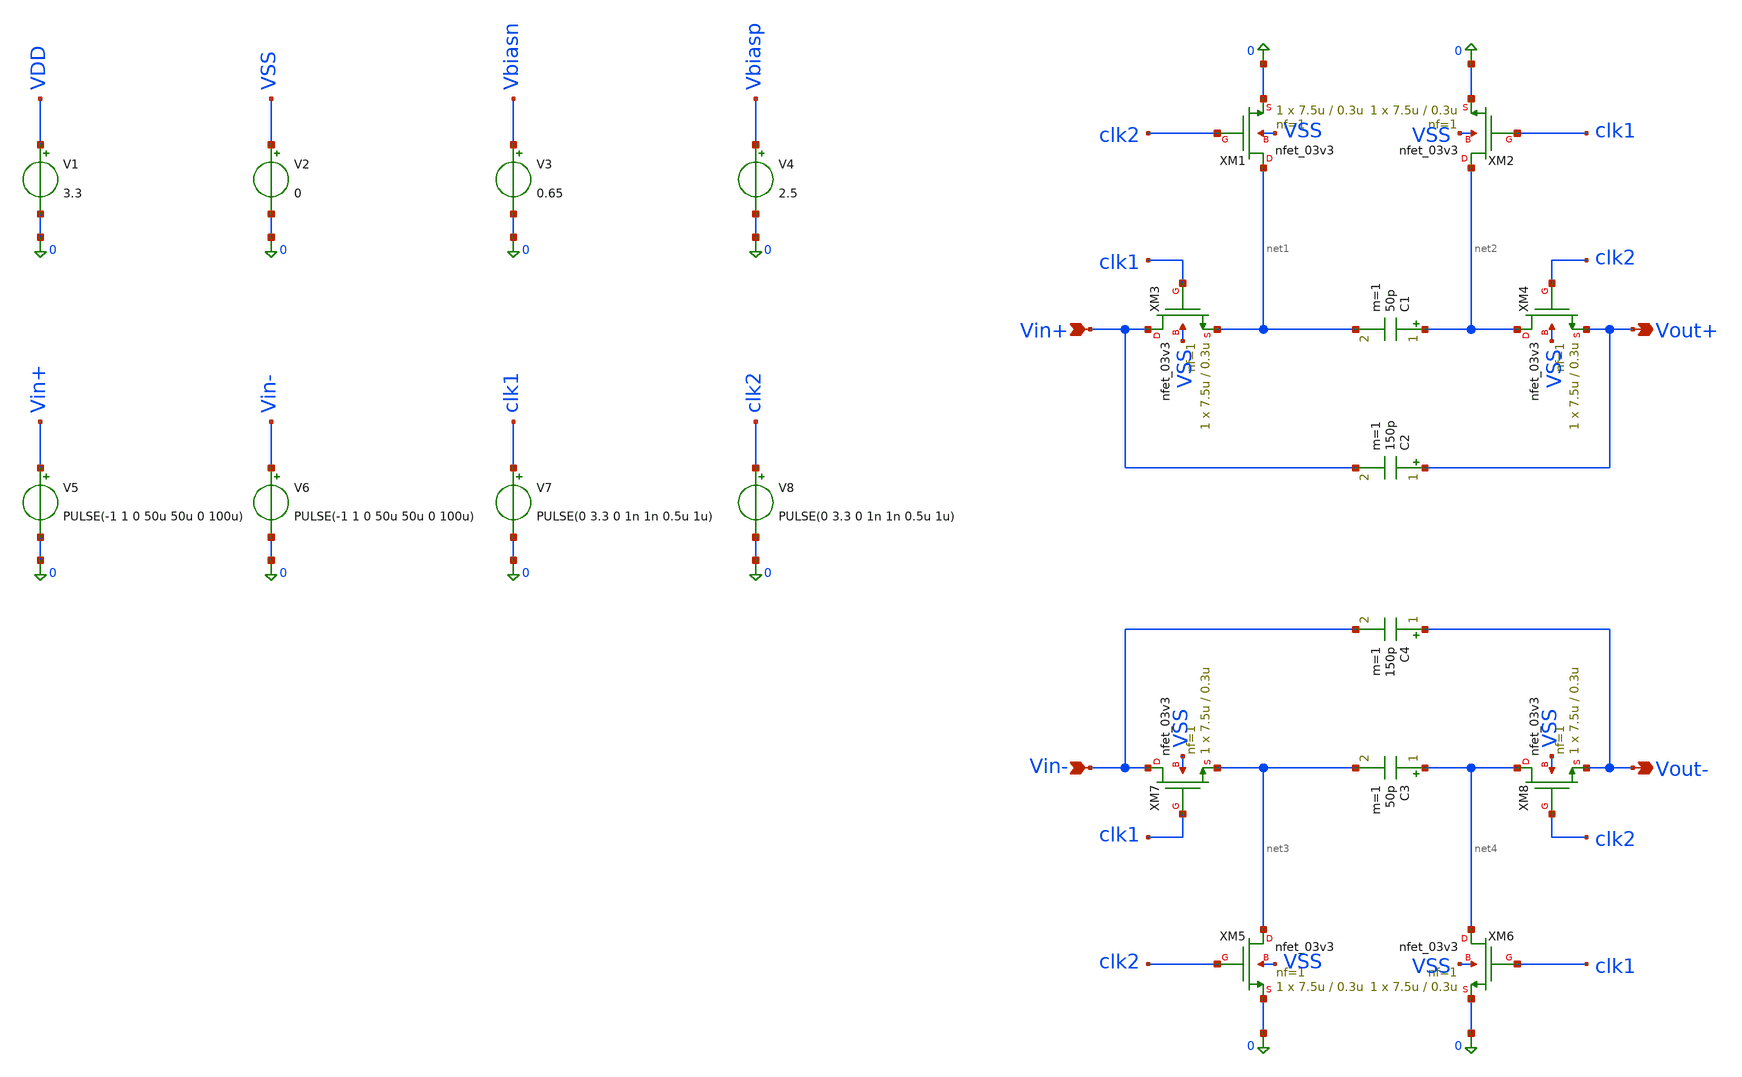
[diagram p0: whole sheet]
** sch_path: src/schematics/integrator_first_order/integrator.sch
**.subckt integrator Vin+ Vin- Vout+ Vout-
*.ipin Vin+
*.ipin Vin-
*.opin Vout+
*.opin Vout-
XM1 net1 clk2 0 VSS nfet_03v3 L=0.3u W=7.5u nf=1 ad='int((nf+1)/2) * W/nf * 0.18u' as='int((nf+2)/2) * W/nf * 0.18u'
+ pd='2*int((nf+1)/2) * (W/nf + 0.18u)' ps='2*int((nf+2)/2) * (W/nf + 0.18u)' nrd='0.18u / W' nrs='0.18u / W'
+ sa=0 sb=0 sd=0 m=1
XM2 net2 clk1 0 VSS nfet_03v3 L=0.3u W=7.5u nf=1 ad='int((nf+1)/2) * W/nf * 0.18u' as='int((nf+2)/2) * W/nf * 0.18u'
+ pd='2*int((nf+1)/2) * (W/nf + 0.18u)' ps='2*int((nf+2)/2) * (W/nf + 0.18u)' nrd='0.18u / W' nrs='0.18u / W'
+ sa=0 sb=0 sd=0 m=1
XM3 Vin+ clk1 net1 VSS nfet_03v3 L=0.3u W=7.5u nf=1 ad='int((nf+1)/2) * W/nf * 0.18u' as='int((nf+2)/2) * W/nf * 0.18u'
+ pd='2*int((nf+1)/2) * (W/nf + 0.18u)' ps='2*int((nf+2)/2) * (W/nf + 0.18u)' nrd='0.18u / W' nrs='0.18u / W'
+ sa=0 sb=0 sd=0 m=1
XM4 net2 clk2 Vout+ VSS nfet_03v3 L=0.3u W=7.5u nf=1 ad='int((nf+1)/2) * W/nf * 0.18u' as='int((nf+2)/2) * W/nf * 0.18u'
+ pd='2*int((nf+1)/2) * (W/nf + 0.18u)' ps='2*int((nf+2)/2) * (W/nf + 0.18u)' nrd='0.18u / W' nrs='0.18u / W'
+ sa=0 sb=0 sd=0 m=1
C1 net2 net1 50p m=1
C2 Vout+ Vin+ 150p m=1
XM5 net3 clk2 0 VSS nfet_03v3 L=0.3u W=7.5u nf=1 ad='int((nf+1)/2) * W/nf * 0.18u' as='int((nf+2)/2) * W/nf * 0.18u'
+ pd='2*int((nf+1)/2) * (W/nf + 0.18u)' ps='2*int((nf+2)/2) * (W/nf + 0.18u)' nrd='0.18u / W' nrs='0.18u / W'
+ sa=0 sb=0 sd=0 m=1
XM6 net4 clk1 0 VSS nfet_03v3 L=0.3u W=7.5u nf=1 ad='int((nf+1)/2) * W/nf * 0.18u' as='int((nf+2)/2) * W/nf * 0.18u'
+ pd='2*int((nf+1)/2) * (W/nf + 0.18u)' ps='2*int((nf+2)/2) * (W/nf + 0.18u)' nrd='0.18u / W' nrs='0.18u / W'
+ sa=0 sb=0 sd=0 m=1
XM7 Vin- clk1 net3 VSS nfet_03v3 L=0.3u W=7.5u nf=1 ad='int((nf+1)/2) * W/nf * 0.18u' as='int((nf+2)/2) * W/nf * 0.18u'
+ pd='2*int((nf+1)/2) * (W/nf + 0.18u)' ps='2*int((nf+2)/2) * (W/nf + 0.18u)' nrd='0.18u / W' nrs='0.18u / W'
+ sa=0 sb=0 sd=0 m=1
XM8 net4 clk2 Vout- VSS nfet_03v3 L=0.3u W=7.5u nf=1 ad='int((nf+1)/2) * W/nf * 0.18u' as='int((nf+2)/2) * W/nf * 0.18u'
+ pd='2*int((nf+1)/2) * (W/nf + 0.18u)' ps='2*int((nf+2)/2) * (W/nf + 0.18u)' nrd='0.18u / W' nrs='0.18u / W'
+ sa=0 sb=0 sd=0 m=1
C3 net4 net3 50p m=1
C4 Vout- Vin- 150p m=1
V1 VDD 0 3.3
V2 VSS 0 0
V3 Vbiasn 0 0.65
V4 Vbiasp 0 2.5
V5 Vin+ 0 PULSE(-1 1 0 50u 50u 0 100u)
V6 Vin- 0 PULSE(-1 1 0 50u 50u 0 100u)
V7 clk1 0 PULSE(0 3.3 0 1n 1n 0.5u 1u)
V8 clk2 0 PULSE(0 3.3 0 1n 1n 0.5u 1u)
**.ends
.end
